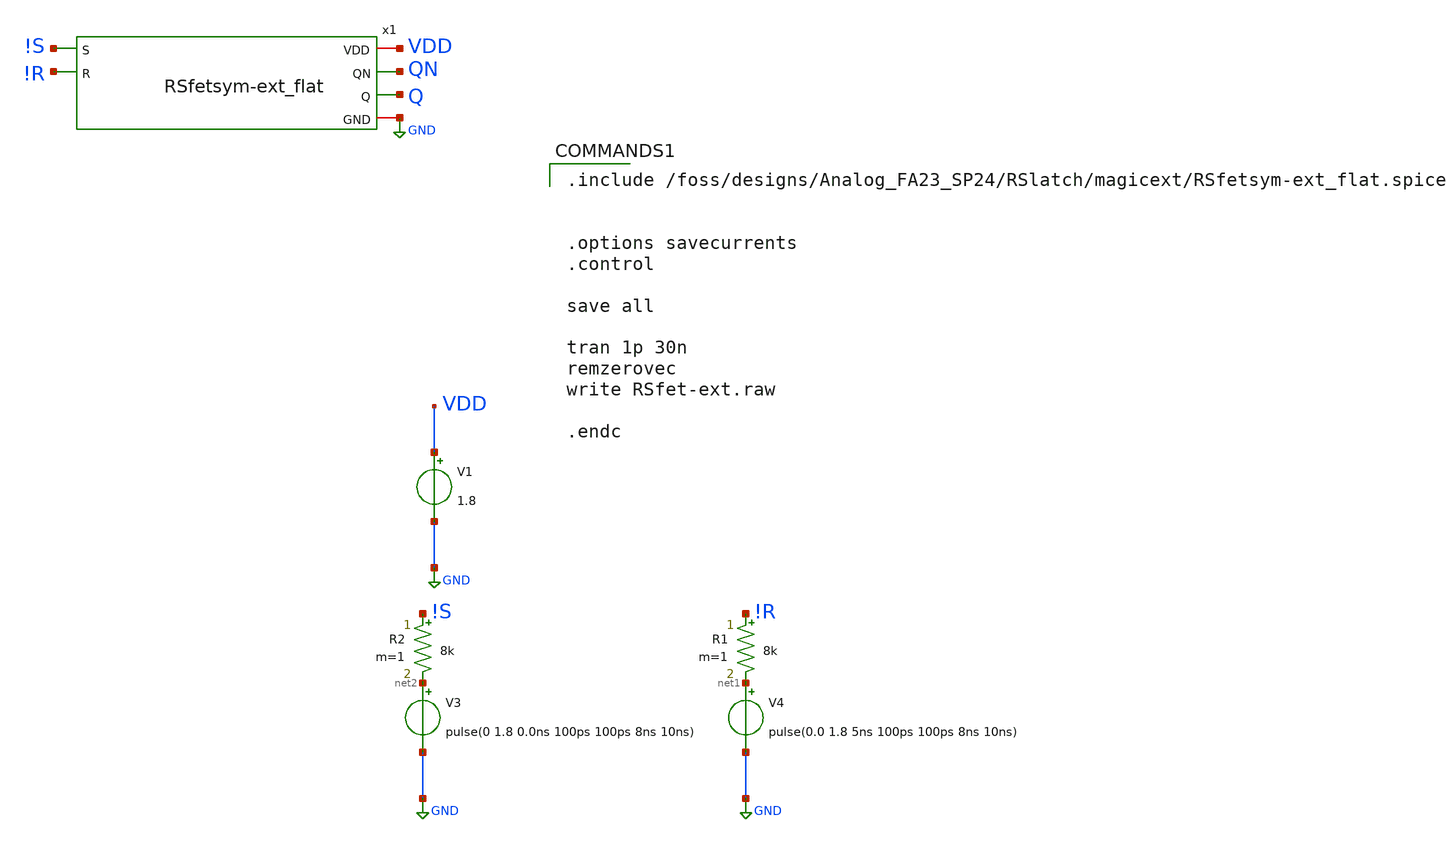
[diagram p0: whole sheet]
** sch_path: RSlatch/xschem/RSfet-ext.sch
.lib $::SKYWATER_MODELS/sky130.lib.spice tt
.include $::SKYWATER_STDCELLS/sky130_fd_sc_hd.spice

**.subckt RSfet-ext
V1 VDD GND 1.8
V4 net1 GND pulse(0.0 1.8 5ns 100ps 100ps 8ns 10ns)
V3 net2 GND pulse(0 1.8 0.0ns 100ps 100ps 8ns 10ns)
R1 !R net1 8k m=1
R2 !S net2 8k m=1
x1 VDD !S !R QN Q GND RSfetsym-ext_flat
**** begin user architecture code

.include /foss/designs/Analog_FA23_SP24/RSlatch/magicext/RSfetsym-ext_flat.spice


.options savecurrents
.control

save all

tran 1p 30n
remzerovec
write RSfet-ext.raw

.endc


**** end user architecture code
**.ends
.GLOBAL GND
.end
